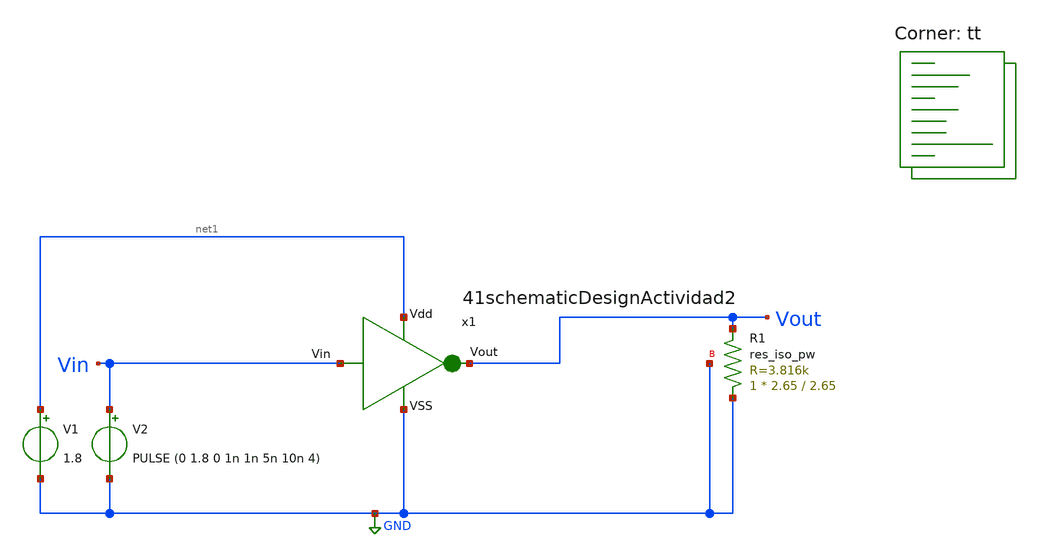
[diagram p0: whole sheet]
** sch_path: trabajosPracticos/tp6/archivosXschem/42simulation.sch
**.subckt 42simulation
V1 net1 GND 1.8
V2 Vin GND PULSE (0 1.8 0 1n 1n 5n 10n 4)
XR1 GND Vout GND sky130_fd_pr__res_iso_pw W=2.65 L=2.65 m=1
x1 net1 Vin Vout GND 41schematicDesignActividad2
**** begin user architecture code
.lib $::SKYWATER_MODELS/sky130.lib.spice tt


.control
	tran 0.5n 400
.endc
.save all



.lib /home/marcosgatica/pdk/ciel/sky130/versions/0fe599b2afb6708d281543108caf8310912f54af/sky130A/libs.tech/ngspice/sky130.lib.spice tt

**** end user architecture code
**.ends

* expanding   symbol:
*+  /home/marcosgatica/facultadUTN/dispositivosElectronicos/trabajosPracticos/tp6/archivosXschem/41schematicDesignActividad2.sym # of pins=4
** sym_path: trabajosPracticos/tp6/archivosXschem/41schematicDesignActividad2.sym
** sch_path: trabajosPracticos/tp6/archivosXschem/41schematicDesignActividad2.sch
.subckt 41schematicDesignActividad2 Vdd Vin Vout VSS
*.ipin Vdd
*.ipin Vin
*.ipin VSS
*.opin Vout
XM1 Vout Vin VSS VSS sky130_fd_pr__nfet_01v8 L=0.15 W=1.05 nf=1 ad='int((nf+1)/2) * W/nf * 0.29' as='int((nf+2)/2) * W/nf * 0.29'
+ pd='2*int((nf+1)/2) * (W/nf + 0.29)' ps='2*int((nf+2)/2) * (W/nf + 0.29)' nrd='0.29 / W' nrs='0.29 / W'
+ sa=0 sb=0 sd=0 mult=1 m=1
XM2 Vout Vin Vdd Vdd sky130_fd_pr__pfet_01v8 L=0.15 W=2.1 nf=1 ad='int((nf+1)/2) * W/nf * 0.29' as='int((nf+2)/2) * W/nf * 0.29'
+ pd='2*int((nf+1)/2) * (W/nf + 0.29)' ps='2*int((nf+2)/2) * (W/nf + 0.29)' nrd='0.29 / W' nrs='0.29 / W'
+ sa=0 sb=0 sd=0 mult=1 m=1
.ends

.GLOBAL GND
.end
